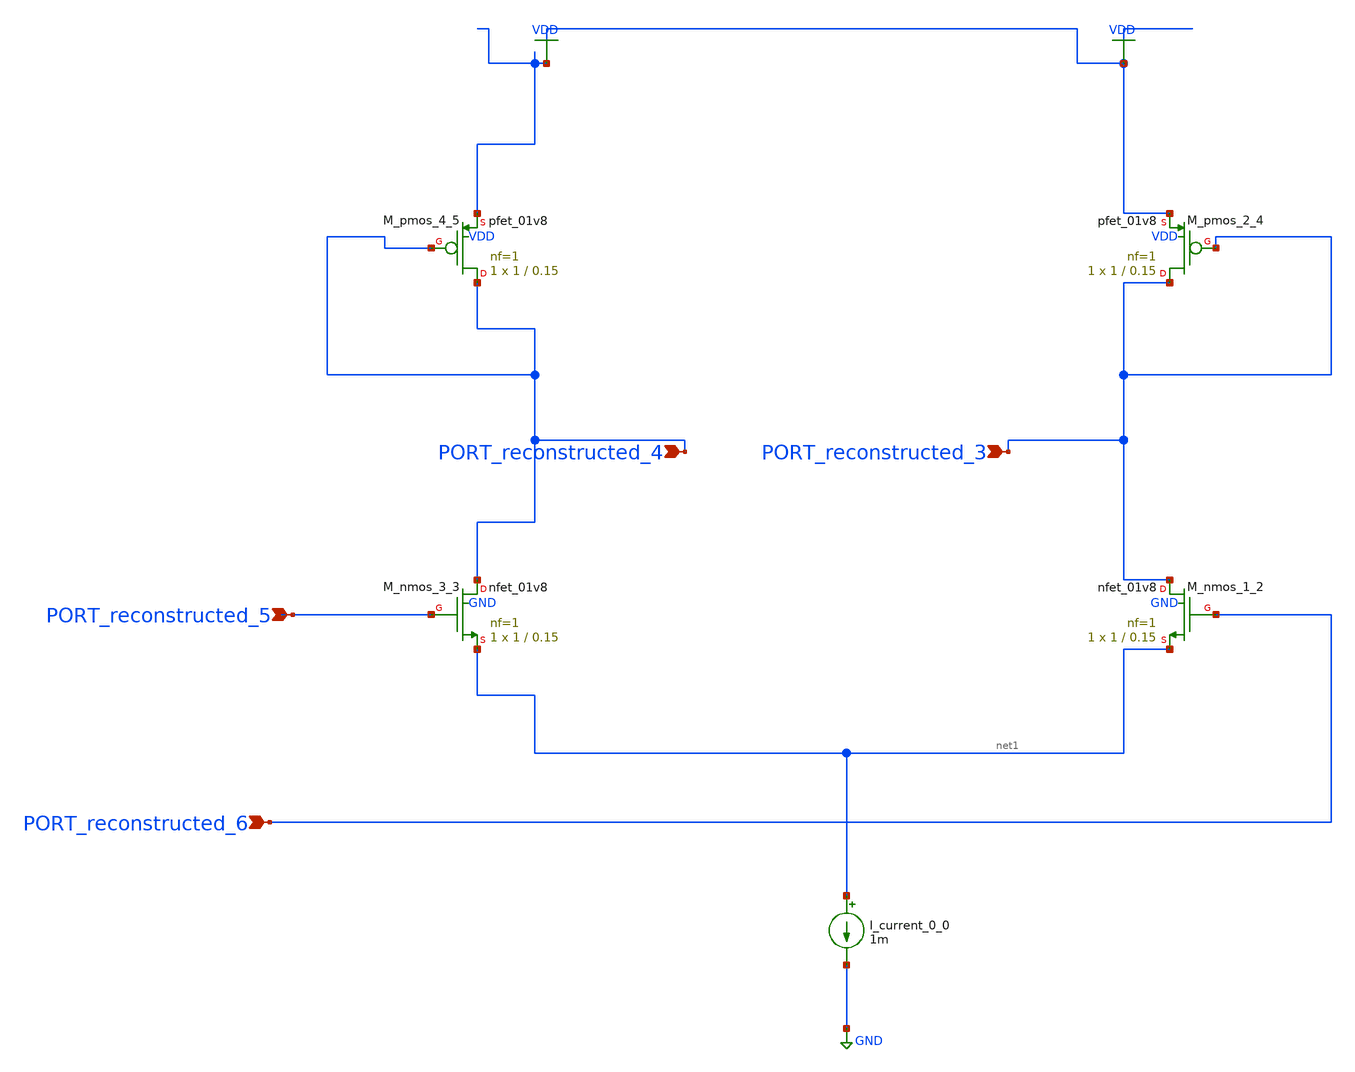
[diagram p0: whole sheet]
** sch_path: schematics/AMSNet/220.sch
**.subckt 220 PORT_reconstructed_3 PORT_reconstructed_4 PORT_reconstructed_5 PORT_reconstructed_6
*.ipin PORT_reconstructed_3
*.ipin PORT_reconstructed_4
*.ipin PORT_reconstructed_5
*.ipin PORT_reconstructed_6
I_current_0_0 net1 GND 1m
XM_nmos_1_2 PORT_reconstructed_3 PORT_reconstructed_6 net1 GND sky130_fd_pr__nfet_01v8 L=0.15 W=1 nf=1
+ ad='int((1 + 1)/2) * 1 / 1 * 0.29' as='int((1 + 2)/2) * 1 / 1 * 0.29' pd='2*int((1 + 1)/2) * (1 / 1 + 0.29)'
+ ps='2*int((1 + 2)/2) * (1 / 1 + 0.29)' nrd='0.29 / 1 ' nrs='0.29 / 1 ' sa=0 sb=0 sd=0 mult=1 m=1
XM_nmos_3_3 PORT_reconstructed_4 PORT_reconstructed_5 net1 GND sky130_fd_pr__nfet_01v8 L=0.15 W=1 nf=1
+ ad='int((1 + 1)/2) * 1 / 1 * 0.29' as='int((1 + 2)/2) * 1 / 1 * 0.29' pd='2*int((1 + 1)/2) * (1 / 1 + 0.29)'
+ ps='2*int((1 + 2)/2) * (1 / 1 + 0.29)' nrd='0.29 / 1 ' nrs='0.29 / 1 ' sa=0 sb=0 sd=0 mult=1 m=1
XM_pmos_2_4 PORT_reconstructed_3 PORT_reconstructed_3 VDD VDD sky130_fd_pr__pfet_01v8 L=0.15 W=1 nf=1
+ ad='int((1 + 1)/2) * 1 / 1 * 0.29' as='int((1 + 2)/2) * 1 / 1 * 0.29' pd='2*int((1 + 1)/2) * (1 / 1 + 0.29)'
+ ps='2*int((1 + 2)/2) * (1 / 1 + 0.29)' nrd='0.29 / 1 ' nrs='0.29 / 1 ' sa=0 sb=0 sd=0 mult=1 m=1
XM_pmos_4_5 PORT_reconstructed_4 PORT_reconstructed_4 VDD VDD sky130_fd_pr__pfet_01v8 L=0.15 W=1 nf=1
+ ad='int((1 + 1)/2) * 1 / 1 * 0.29' as='int((1 + 2)/2) * 1 / 1 * 0.29' pd='2*int((1 + 1)/2) * (1 / 1 + 0.29)'
+ ps='2*int((1 + 2)/2) * (1 / 1 + 0.29)' nrd='0.29 / 1 ' nrs='0.29 / 1 ' sa=0 sb=0 sd=0 mult=1 m=1
**.ends
.GLOBAL GND
.GLOBAL VDD
.end
